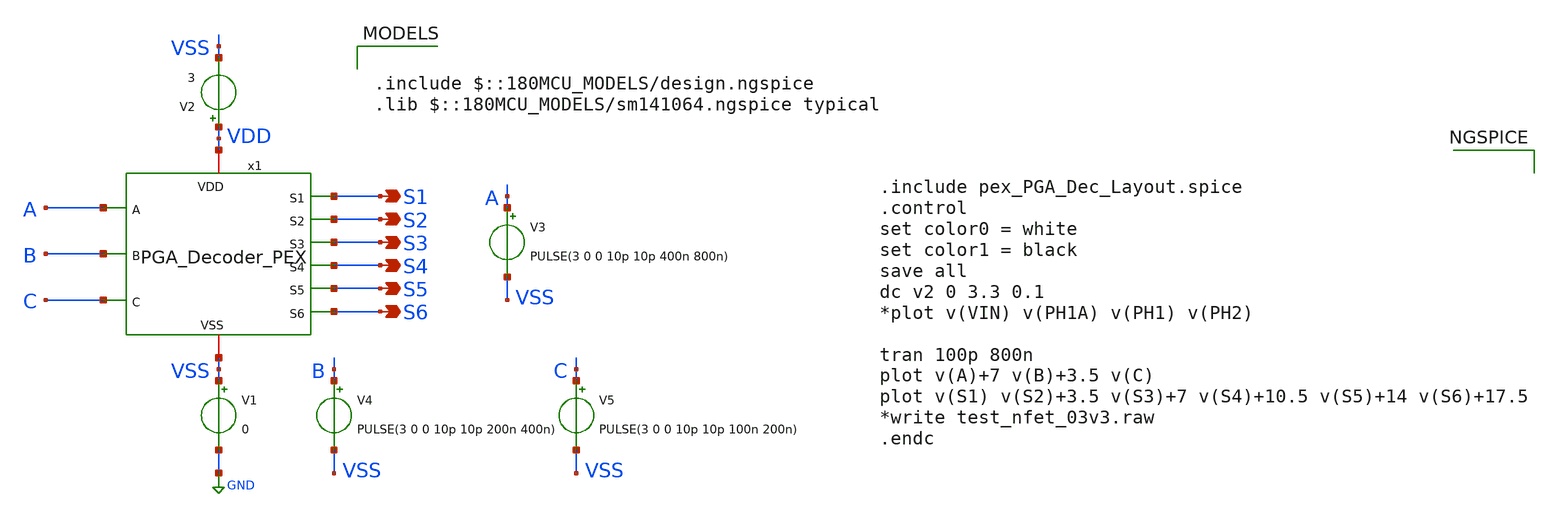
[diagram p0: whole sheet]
** sch_path: SCOP_INPUT_AND_MUX_PAKISTAN_03/Xschem/PGA_Decoder/PGA_Decoder_TB.sch
**.subckt PGA_Decoder_TB S1 S2 S3 S4 S5 S6
*.opin S1
*.opin S2
*.opin S3
*.opin S4
*.opin S5
*.opin S6
V1 VSS GND 0
V2 VDD VSS 3
V3 A VSS PULSE(3 0 0 10p 10p 400n 800n)
V4 B VSS PULSE(3 0 0 10p 10p 200n 400n)
V5 C VSS PULSE(3 0 0 10p 10p 100n 200n)
x1 S2 S3 S1 VDD A S6 B S4 C VSS S5 PGA_Decoder_PEX
**** begin user architecture code

.include $::180MCU_MODELS/design.ngspice
.lib $::180MCU_MODELS/sm141064.ngspice typical



.include pex_PGA_Dec_Layout.spice
.control
set color0 = white
set color1 = black
save all
dc v2 0 3.3 0.1
*plot v(VIN) v(PH1A) v(PH1) v(PH2)

tran 100p 800n
plot v(A)+7 v(B)+3.5 v(C)
plot v(S1) v(S2)+3.5 v(S3)+7 v(S4)+10.5 v(S5)+14 v(S6)+17.5
*write test_nfet_03v3.raw
.endc


**** end user architecture code
**.ends
.GLOBAL GND
.end
